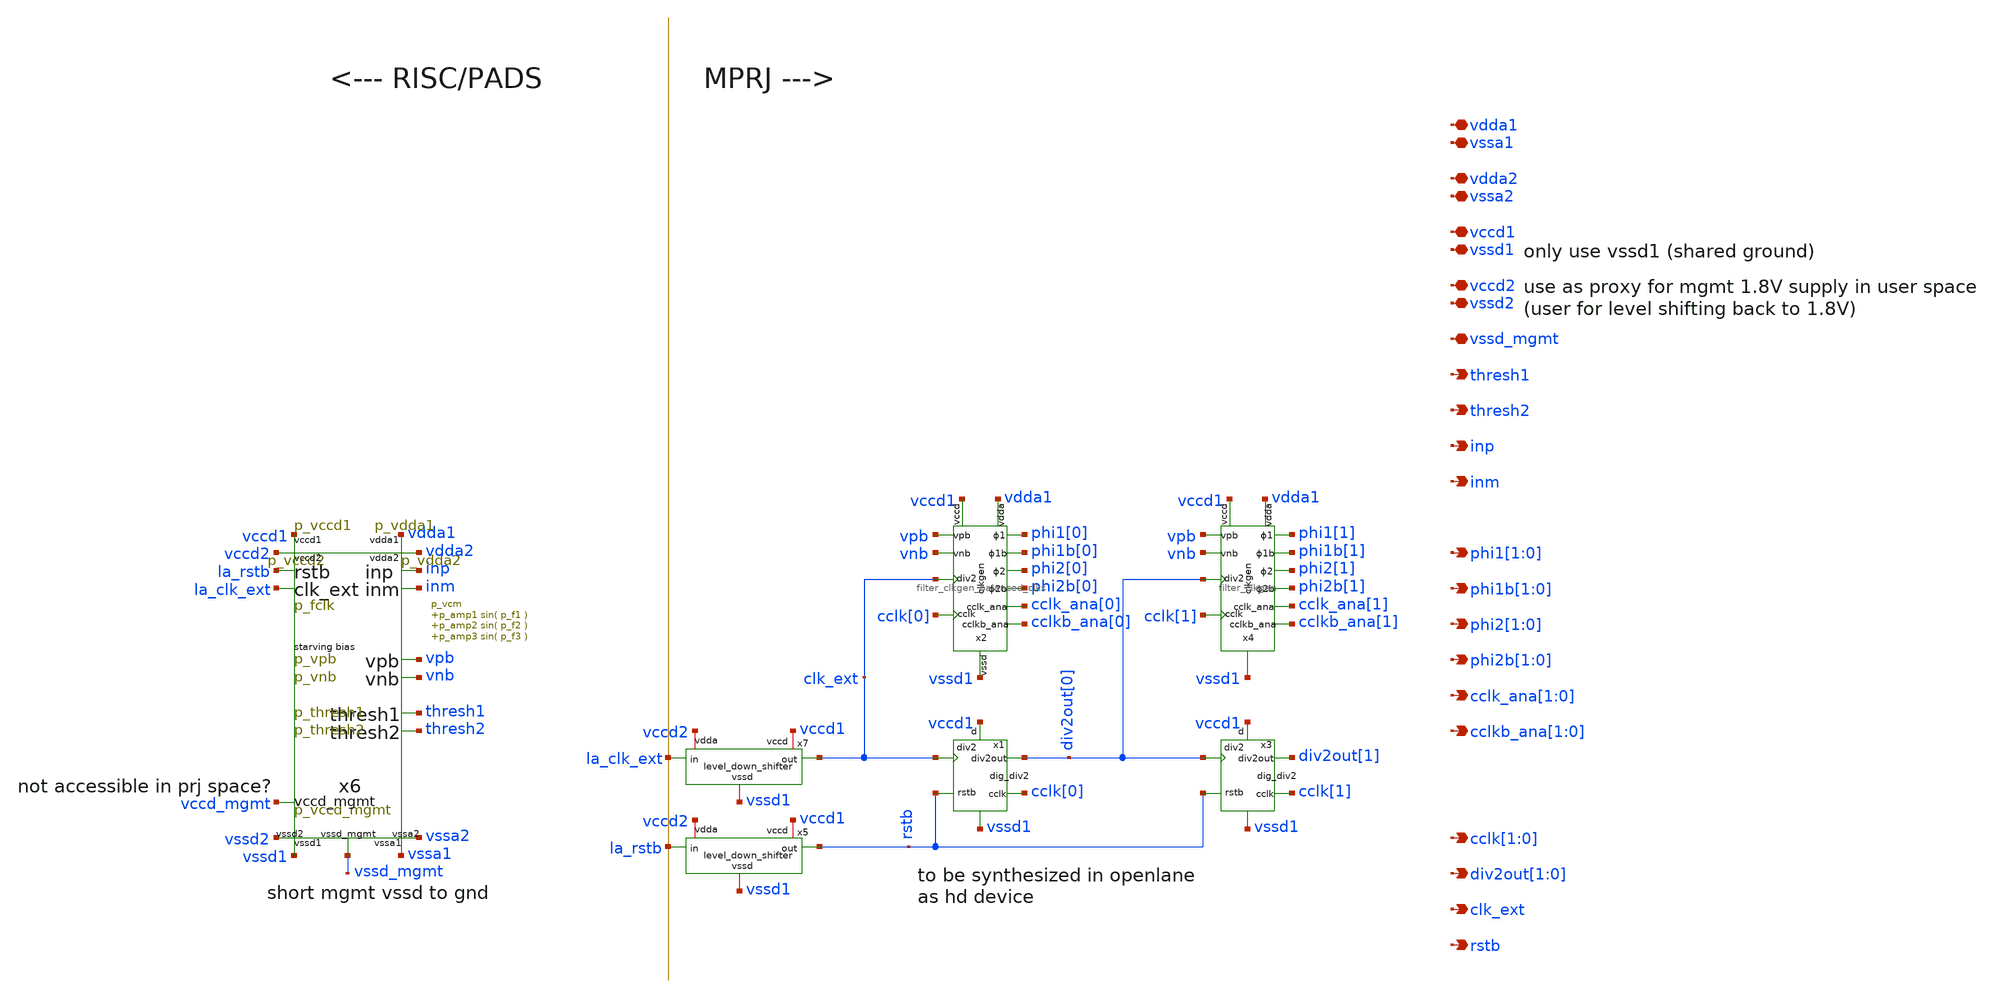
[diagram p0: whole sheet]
** sch_path: xschem/test_bench/risc_signals.sch
**.subckt risc_signals thresh1 thresh2 inp inm phi1[1],phi1[0] phi1b[1],phi1b[0]
*+ div2out[1],div2out[0] rstb phi2[1],phi2[0] phi2b[1],phi2b[0] cclk_ana[1],cclk_ana[0] cclkb_ana[1],cclkb_ana[0] clk_ext
*+ cclk[1],cclk[0] vccd1 vssd1 vdda1 vssa1 vdda2 vssa2 vccd2 vssd2 vssd_mgmt
*.opin thresh1
*.opin thresh2
*.opin inp
*.opin inm
*.opin phi1[1],phi1[0]
*.opin phi1b[1],phi1b[0]
*.opin div2out[1],div2out[0]
*.opin rstb
*.opin phi2[1],phi2[0]
*.opin phi2b[1],phi2b[0]
*.opin cclk_ana[1],cclk_ana[0]
*.opin cclkb_ana[1],cclkb_ana[0]
*.opin clk_ext
*.opin cclk[1],cclk[0]
*.iopin vccd1
*.iopin vssd1
*.iopin vdda1
*.iopin vssa1
*.iopin vdda2
*.iopin vssa2
*.iopin vccd2
*.iopin vssd2
*.iopin vssd_mgmt
x4 cclk[1] phi2b[1] phi2[1] phi1b[1] phi1[1] cclkb_ana[1] cclk_ana[1] vpb vnb vdda1 vssd1 vccd1
+ div2out[0] filter_clkgen
x6 thresh1 thresh2 vdda1 vssa1 inp inm la_clk_ext la_rstb vccd1 vssd1 vpb vnb vccd_mgmt vssd_mgmt
+ vccd2 vdda2 vssd2 vssa2 pad_frame p_vdda1=p_vdda1 p_vdda2=p_vdda2 p_vccd1=p_vccd1 p_vccd2=p_vccd2
+ p_vccd_mgmt=p_vccd_mgmt p_fclk=p_fclk p_duty_cycle=p_duty_cycle p_rstb_delay=p_rstb_delay p_rstb_tr=p_rstb_tr
+ p_thresh1=p_thresh1 p_thresh2=p_thresh2 p_vpb=p_vpb p_vnb=p_vnb p_vcm=p_vcm p_amp1=p_amp1 p_f1=p_f1 p_amp2=p_amp2
+ p_f2=p_f2 p_amp3=p_amp3 p_f3=p_f3
x1 rstb cclk[0] div2out[0] vccd1 vssd1 clk_ext dig_div2
x3 rstb cclk[1] div2out[1] vccd1 vssd1 div2out[0] dig_div2
x5 vccd2 vccd1 la_rstb rstb vssd1 level_down_shifter
x7 vccd2 vccd1 la_clk_ext clk_ext vssd1 level_down_shifter
x2 cclk[0] phi2b[0] phi2[0] phi1b[0] phi1[0] cclkb_ana[0] cclk_ana[0] vpb vnb vdda1 vssd1 vccd1
+ clk_ext filter_clkgen_balanced_clks
**.ends
.end
